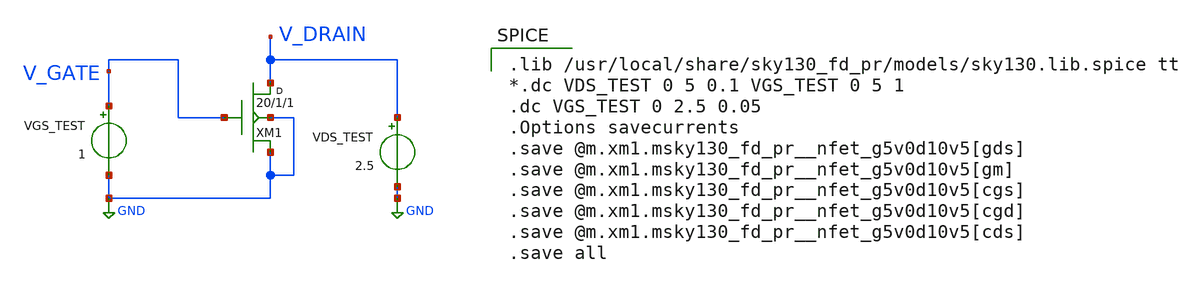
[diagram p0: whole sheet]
** sch_path: images/foss-asic-tools/addons/examples/sky130-analog/device/sims/fet_sweep.sch
**.subckt fet_sweep
VGS_TEST V_GATE GND 1
XM1 V_DRAIN V_GATE GND GND sky130_fd_pr__nfet_g5v0d10v5 w=20 l=1 m=1
VDS_TEST V_DRAIN GND 2.5
**** begin user architecture code

.lib /usr/local/share/sky130_fd_pr/models/sky130.lib.spice tt
*.dc VDS_TEST 0 5 0.1 VGS_TEST 0 5 1
.dc VGS_TEST 0 2.5 0.05
.Options savecurrents
.save @m.xm1.msky130_fd_pr__nfet_g5v0d10v5[gds]
.save @m.xm1.msky130_fd_pr__nfet_g5v0d10v5[gm]
.save @m.xm1.msky130_fd_pr__nfet_g5v0d10v5[cgs]
.save @m.xm1.msky130_fd_pr__nfet_g5v0d10v5[cgd]
.save @m.xm1.msky130_fd_pr__nfet_g5v0d10v5[cds]
.save all

**** end user architecture code
**.ends
.GLOBAL GND
.end
